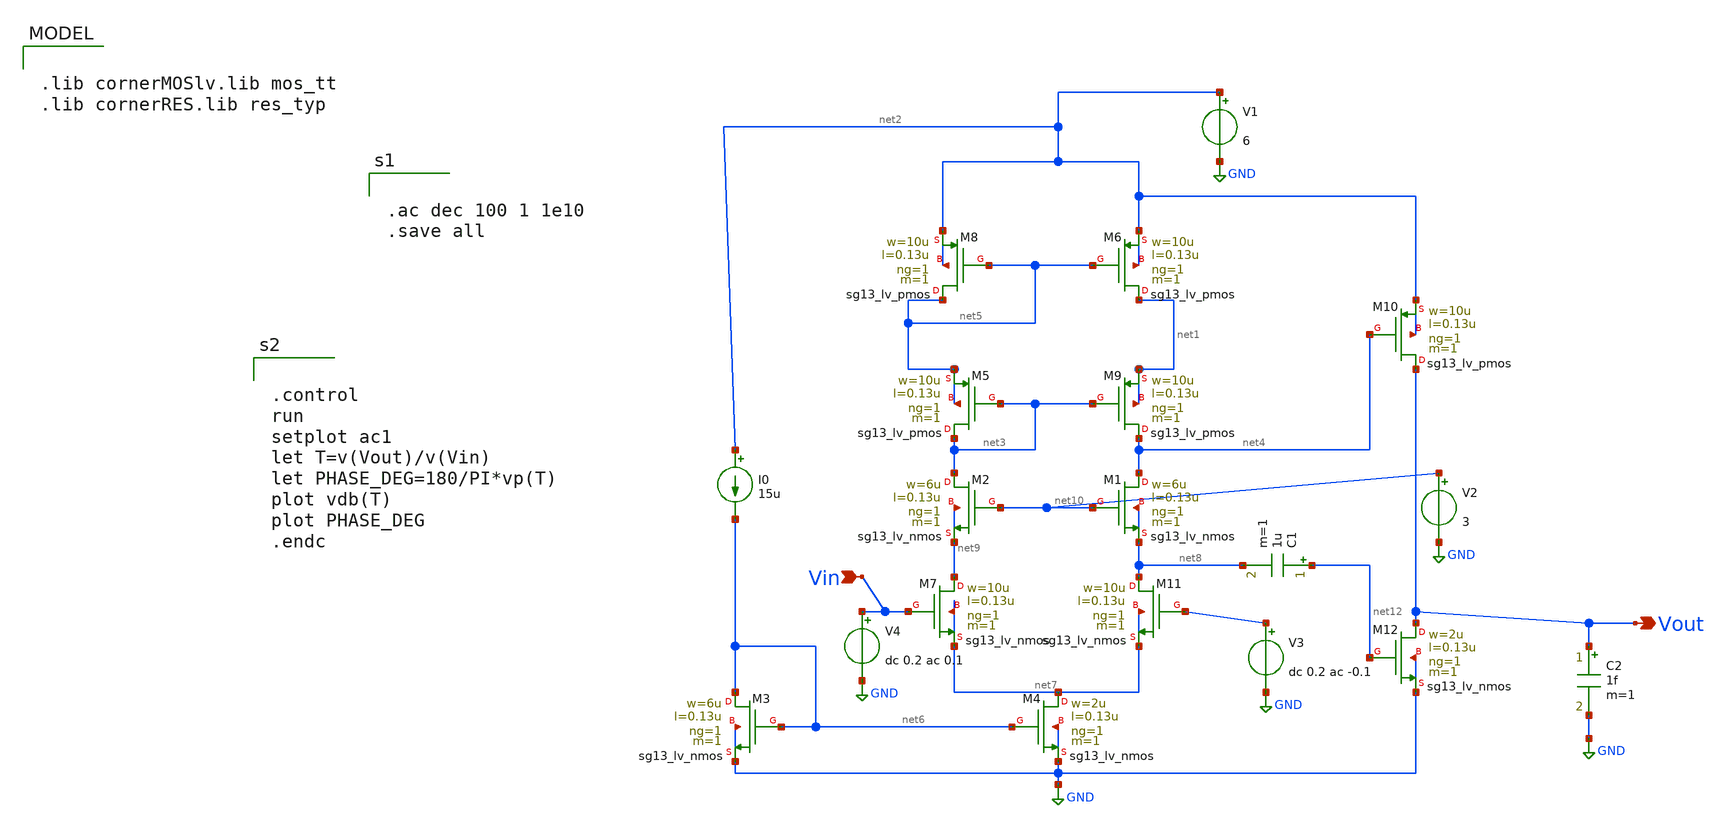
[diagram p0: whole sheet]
** sch_path: Telescopic_Twostage.sch
**.subckt Telescopic_Twostage Vout Vin
*.opin Vout
*.ipin Vin
I0 net2 net6 15u
XM7 net9 Vin net7 net7 sg13_lv_nmos w=10u l=0.13u ng=1 m=1 mm_ok=1
XM11 net8 net11 net7 net7 sg13_lv_nmos w=10u l=0.13u ng=1 m=1 mm_ok=1
XM1 net4 net10 net8 net8 sg13_lv_nmos w=6u l=0.13u ng=1 m=1 mm_ok=1
XM2 net3 net10 net9 net9 sg13_lv_nmos w=6u l=0.13u ng=1 m=1 mm_ok=1
XM3 net6 net6 GND GND sg13_lv_nmos w=6u l=0.13u ng=1 m=1 mm_ok=1
XM4 net7 net6 GND GND sg13_lv_nmos w=2u l=0.13u ng=1 m=1 mm_ok=1
XM9 net4 net3 net1 net1 sg13_lv_pmos w=10u l=0.13u ng=1 m=1 mm_ok=1
XM6 net1 net5 net2 net2 sg13_lv_pmos w=10u l=0.13u ng=1 m=1 mm_ok=1
XM5 net3 net3 net5 net5 sg13_lv_pmos w=10u l=0.13u ng=1 m=1 mm_ok=1
XM8 net5 net5 net2 net2 sg13_lv_pmos w=10u l=0.13u ng=1 m=1 mm_ok=1
V1 net2 GND 6
V3 net11 GND dc 0.2 ac -0.1
V4 Vin GND dc 0.2 ac 0.1
XM10 Vout net4 net2 net2 sg13_lv_pmos w=10u l=0.13u ng=1 m=1 mm_ok=1
XM12 Vout net12 GND GND sg13_lv_nmos w=2u l=0.13u ng=1 m=1 mm_ok=1
C1 net12 net8 1u m=1
C2 Vout GND 1f m=1
V2 net10 GND 3
**** begin user architecture code


.ac dec 100 1 1e10
.save all




.control
run
setplot ac1
let T=v(Vout)/v(Vin)
let PHASE_DEG=180/PI*vp(T)
plot vdb(T)
plot PHASE_DEG
.endc



.lib cornerMOSlv.lib mos_tt
.lib cornerRES.lib res_typ

**** end user architecture code
**.ends
.GLOBAL GND
.end
